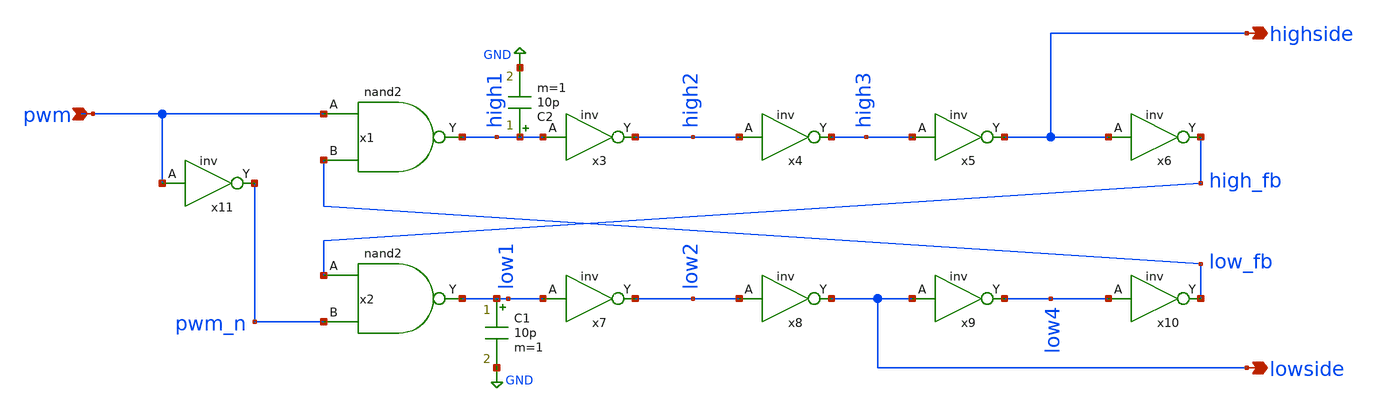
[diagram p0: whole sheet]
** sch_path: Ene_Thompson/deadtime.sch
**.subckt deadtime pwm highside lowside
*.ipin pwm
*.opin highside
*.opin lowside
x1 pwm low_fb high1 nand2
x2 high_fb pwm_n low1 nand2
x3 high1 high2 inv
x4 high2 high3 inv
x5 high3 highside inv
x6 highside high_fb inv
x7 low1 low2 inv
x8 low2 lowside inv
x9 lowside low4 inv
x10 low4 low_fb inv
x11 pwm pwm_n inv
C1 low1 GND 10p m=1
C2 high1 GND 10p m=1
**.ends

* expanding   symbol:  nand2.sym # of pins=3
** sym_path: Ene_Thompson/nand2.sym
** sch_path: Ene_Thompson/nand2.sch
.subckt nand2 A B Y
*.ipin A
*.opin Y
*.ipin B
XM1 net1 B GND GND sky130_fd_pr__nfet_g5v0d10v5 L=0.5 W=1 nf=1 ad='int((nf+1)/2) * W/nf * 0.29' as='int((nf+2)/2) * W/nf * 0.29'
+ pd='2*int((nf+1)/2) * (W/nf + 0.29)' ps='2*int((nf+2)/2) * (W/nf + 0.29)' nrd='0.29 / W' nrs='0.29 / W'
+ sa=0 sb=0 sd=0 mult=1 m=1
XM2 Y A VDDH VDDH sky130_fd_pr__pfet_g5v0d10v5 L=0.5 W=1 nf=1 ad='int((nf+1)/2) * W/nf * 0.29' as='int((nf+2)/2) * W/nf * 0.29'
+ pd='2*int((nf+1)/2) * (W/nf + 0.29)' ps='2*int((nf+2)/2) * (W/nf + 0.29)' nrd='0.29 / W' nrs='0.29 / W'
+ sa=0 sb=0 sd=0 mult=1 m=1
XM3 Y B VDDH VDDH sky130_fd_pr__pfet_g5v0d10v5 L=0.5 W=1 nf=1 ad='int((nf+1)/2) * W/nf * 0.29' as='int((nf+2)/2) * W/nf * 0.29'
+ pd='2*int((nf+1)/2) * (W/nf + 0.29)' ps='2*int((nf+2)/2) * (W/nf + 0.29)' nrd='0.29 / W' nrs='0.29 / W'
+ sa=0 sb=0 sd=0 mult=1 m=1
XM4 Y A net1 GND sky130_fd_pr__nfet_g5v0d10v5 L=0.5 W=1 nf=1 ad='int((nf+1)/2) * W/nf * 0.29' as='int((nf+2)/2) * W/nf * 0.29'
+ pd='2*int((nf+1)/2) * (W/nf + 0.29)' ps='2*int((nf+2)/2) * (W/nf + 0.29)' nrd='0.29 / W' nrs='0.29 / W'
+ sa=0 sb=0 sd=0 mult=1 m=1
.ends


* expanding   symbol:  inv.sym # of pins=2
** sym_path: Ene_Thompson/inv.sym
** sch_path: Ene_Thompson/inv.sch
.subckt inv A Y
*.ipin A
*.opin Y
XM1 Y A GND GND sky130_fd_pr__nfet_g5v0d10v5 L=0.5 W=1 nf=1 ad='int((nf+1)/2) * W/nf * 0.29' as='int((nf+2)/2) * W/nf * 0.29'
+ pd='2*int((nf+1)/2) * (W/nf + 0.29)' ps='2*int((nf+2)/2) * (W/nf + 0.29)' nrd='0.29 / W' nrs='0.29 / W'
+ sa=0 sb=0 sd=0 mult=1 m=1
XM2 Y A VDDH VDDH sky130_fd_pr__pfet_g5v0d10v5 L=0.5 W=1 nf=1 ad='int((nf+1)/2) * W/nf * 0.29' as='int((nf+2)/2) * W/nf * 0.29'
+ pd='2*int((nf+1)/2) * (W/nf + 0.29)' ps='2*int((nf+2)/2) * (W/nf + 0.29)' nrd='0.29 / W' nrs='0.29 / W'
+ sa=0 sb=0 sd=0 mult=2 m=2
.ends

.GLOBAL GND
.GLOBAL VDDH
.end
